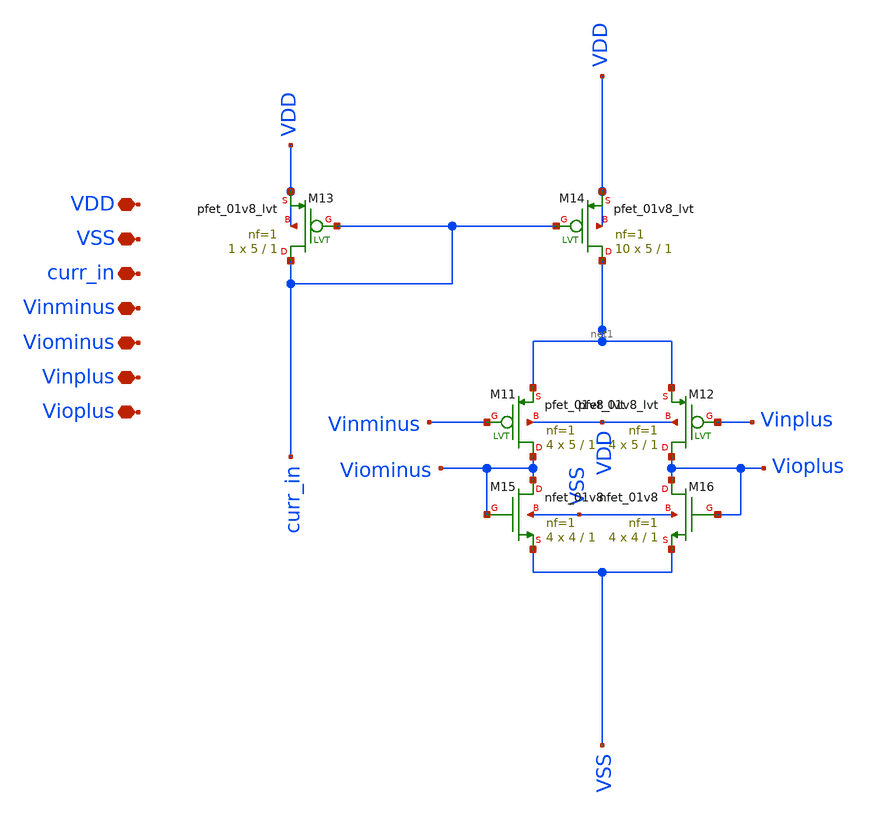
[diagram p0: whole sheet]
** sch_path: xschem/preamp_1.sch
**.subckt preamp_1 VDD VSS curr_in Vinminus Viominus Vinplus Vioplus
*.iopin VDD
*.iopin VSS
*.iopin curr_in
*.iopin Vinminus
*.iopin Viominus
*.iopin Vinplus
*.iopin Vioplus
XM11 Viominus Vinminus net1 VDD sky130_fd_pr__pfet_01v8_lvt L=1 W=5 nf=1 ad='int((nf+1)/2) * W/nf * 0.29'
+ as='int((nf+2)/2) * W/nf * 0.29' pd='2*int((nf+1)/2) * (W/nf + 0.29)' ps='2*int((nf+2)/2) * (W/nf + 0.29)'
+ nrd='0.29 / W' nrs='0.29 / W' sa=0 sb=0 sd=0 mult=4 m=4
XM12 Vioplus Vinplus net1 VDD sky130_fd_pr__pfet_01v8_lvt L=1 W=5 nf=1 ad='int((nf+1)/2) * W/nf * 0.29'
+ as='int((nf+2)/2) * W/nf * 0.29' pd='2*int((nf+1)/2) * (W/nf + 0.29)' ps='2*int((nf+2)/2) * (W/nf + 0.29)'
+ nrd='0.29 / W' nrs='0.29 / W' sa=0 sb=0 sd=0 mult=4 m=4
XM13 curr_in curr_in VDD VDD sky130_fd_pr__pfet_01v8_lvt L=1 W=5 nf=1 ad='int((nf+1)/2) * W/nf * 0.29'
+ as='int((nf+2)/2) * W/nf * 0.29' pd='2*int((nf+1)/2) * (W/nf + 0.29)' ps='2*int((nf+2)/2) * (W/nf + 0.29)'
+ nrd='0.29 / W' nrs='0.29 / W' sa=0 sb=0 sd=0 mult=1 m=1
XM14 net1 curr_in VDD VDD sky130_fd_pr__pfet_01v8_lvt L=1 W=5 nf=1 ad='int((nf+1)/2) * W/nf * 0.29' as='int((nf+2)/2) * W/nf * 0.29'
+ pd='2*int((nf+1)/2) * (W/nf + 0.29)' ps='2*int((nf+2)/2) * (W/nf + 0.29)' nrd='0.29 / W' nrs='0.29 / W'
+ sa=0 sb=0 sd=0 mult=10 m=10
XM15 Viominus Viominus VSS VSS sky130_fd_pr__nfet_01v8 L=1 W=4 nf=1 ad='int((nf+1)/2) * W/nf * 0.29'
+ as='int((nf+2)/2) * W/nf * 0.29' pd='2*int((nf+1)/2) * (W/nf + 0.29)' ps='2*int((nf+2)/2) * (W/nf + 0.29)'
+ nrd='0.29 / W' nrs='0.29 / W' sa=0 sb=0 sd=0 mult=4 m=4
XM16 Vioplus Vioplus VSS VSS sky130_fd_pr__nfet_01v8 L=1 W=4 nf=1 ad='int((nf+1)/2) * W/nf * 0.29' as='int((nf+2)/2) * W/nf * 0.29'
+ pd='2*int((nf+1)/2) * (W/nf + 0.29)' ps='2*int((nf+2)/2) * (W/nf + 0.29)' nrd='0.29 / W' nrs='0.29 / W'
+ sa=0 sb=0 sd=0 mult=4 m=4
**.ends
.end
